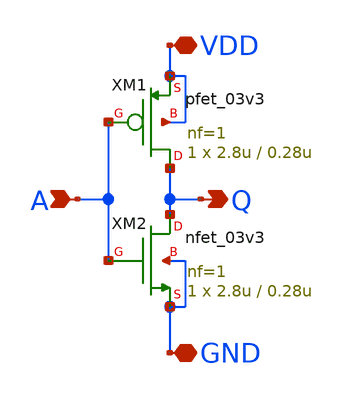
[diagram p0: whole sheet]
** sch_path: review/0407/inverter/inv.sch
**.subckt inv A Q VDD GND
*.ipin A
*.opin Q
*.iopin VDD
*.iopin GND
XM1 Q A VDD VDD pfet_03v3 L=0.28u W=2.8u nf=1 ad='int((nf+1)/2) * W/nf * 0.18u' as='int((nf+2)/2) * W/nf * 0.18u'
+ pd='2*int((nf+1)/2) * (W/nf + 0.18u)' ps='2*int((nf+2)/2) * (W/nf + 0.18u)' nrd='0.18u / W' nrs='0.18u / W'
+ sa=0 sb=0 sd=0 m=1
XM2 Q A GND GND nfet_03v3 L=0.28u W=2.8u nf=1 ad='int((nf+1)/2) * W/nf * 0.18u' as='int((nf+2)/2) * W/nf * 0.18u'
+ pd='2*int((nf+1)/2) * (W/nf + 0.18u)' ps='2*int((nf+2)/2) * (W/nf + 0.18u)' nrd='0.18u / W' nrs='0.18u / W'
+ sa=0 sb=0 sd=0 m=1
**.ends
.end
